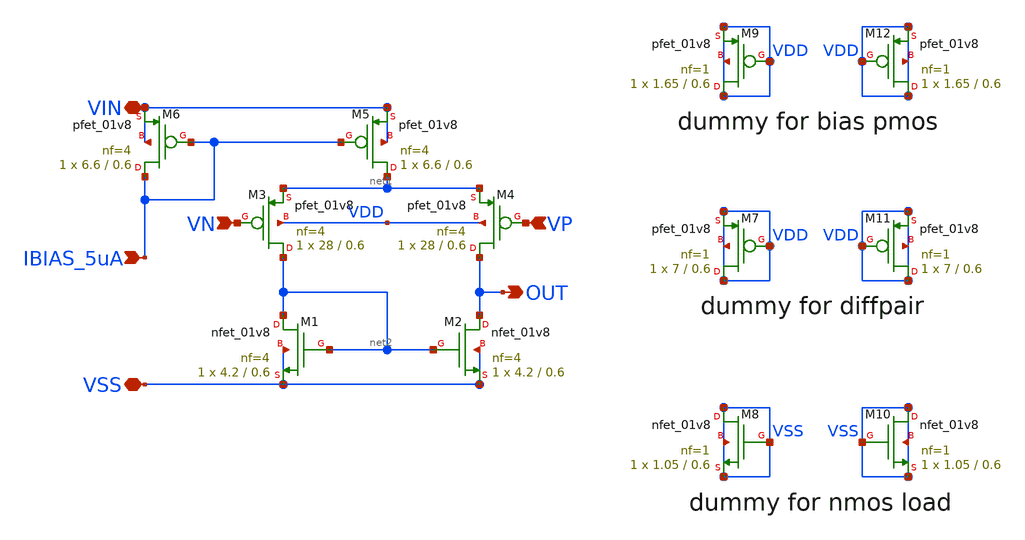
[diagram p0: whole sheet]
** sch_path: xschem/error-amplifier/error-amplifier.sch
**.subckt error-amplifier IBIAS_5uA VN VP VIN VSS OUT
*.ipin IBIAS_5uA
*.ipin VN
*.ipin VP
*.iopin VIN
*.iopin VSS
*.opin OUT
XM1 net2 net2 VSS VSS sky130_fd_pr__nfet_01v8 L=0.6 W=4.2 nf=4 ad='int((nf+1)/2) * W/nf * 0.29' as='int((nf+2)/2) * W/nf * 0.29'
+ pd='2*int((nf+1)/2) * (W/nf + 0.29)' ps='2*int((nf+2)/2) * (W/nf + 0.29)' nrd='0.29 / W' nrs='0.29 / W'
+ sa=0 sb=0 sd=0 mult=1 m=1
XM2 OUT net2 VSS VSS sky130_fd_pr__nfet_01v8 L=0.6 W=4.2 nf=4 ad='int((nf+1)/2) * W/nf * 0.29' as='int((nf+2)/2) * W/nf * 0.29'
+ pd='2*int((nf+1)/2) * (W/nf + 0.29)' ps='2*int((nf+2)/2) * (W/nf + 0.29)' nrd='0.29 / W' nrs='0.29 / W'
+ sa=0 sb=0 sd=0 mult=1 m=1
XM3 net2 VN net1 VDD sky130_fd_pr__pfet_01v8 L=0.6 W=28 nf=4 ad='int((nf+1)/2) * W/nf * 0.29' as='int((nf+2)/2) * W/nf * 0.29'
+ pd='2*int((nf+1)/2) * (W/nf + 0.29)' ps='2*int((nf+2)/2) * (W/nf + 0.29)' nrd='0.29 / W' nrs='0.29 / W'
+ sa=0 sb=0 sd=0 mult=1 m=1
XM4 OUT VP net1 VDD sky130_fd_pr__pfet_01v8 L=0.6 W=28 nf=4 ad='int((nf+1)/2) * W/nf * 0.29' as='int((nf+2)/2) * W/nf * 0.29'
+ pd='2*int((nf+1)/2) * (W/nf + 0.29)' ps='2*int((nf+2)/2) * (W/nf + 0.29)' nrd='0.29 / W' nrs='0.29 / W'
+ sa=0 sb=0 sd=0 mult=1 m=1
XM5 net1 IBIAS_5uA VIN VIN sky130_fd_pr__pfet_01v8 L=0.6 W=6.6 nf=4 ad='int((nf+1)/2) * W/nf * 0.29'
+ as='int((nf+2)/2) * W/nf * 0.29' pd='2*int((nf+1)/2) * (W/nf + 0.29)' ps='2*int((nf+2)/2) * (W/nf + 0.29)'
+ nrd='0.29 / W' nrs='0.29 / W' sa=0 sb=0 sd=0 mult=1 m=1
XM6 IBIAS_5uA IBIAS_5uA VIN VIN sky130_fd_pr__pfet_01v8 L=0.6 W=6.6 nf=4 ad='int((nf+1)/2) * W/nf * 0.29'
+ as='int((nf+2)/2) * W/nf * 0.29' pd='2*int((nf+1)/2) * (W/nf + 0.29)' ps='2*int((nf+2)/2) * (W/nf + 0.29)'
+ nrd='0.29 / W' nrs='0.29 / W' sa=0 sb=0 sd=0 mult=1 m=1
XM7 VDD VDD VDD VDD sky130_fd_pr__pfet_01v8 L=0.6 W=7 nf=1 ad='int((nf+1)/2) * W/nf * 0.29' as='int((nf+2)/2) * W/nf * 0.29'
+ pd='2*int((nf+1)/2) * (W/nf + 0.29)' ps='2*int((nf+2)/2) * (W/nf + 0.29)' nrd='0.29 / W' nrs='0.29 / W'
+ sa=0 sb=0 sd=0 mult=1 m=1
XM8 VSS VSS VSS VSS sky130_fd_pr__nfet_01v8 L=0.6 W=1.05 nf=1 ad='int((nf+1)/2) * W/nf * 0.29' as='int((nf+2)/2) * W/nf * 0.29'
+ pd='2*int((nf+1)/2) * (W/nf + 0.29)' ps='2*int((nf+2)/2) * (W/nf + 0.29)' nrd='0.29 / W' nrs='0.29 / W'
+ sa=0 sb=0 sd=0 mult=1 m=1
XM9 VDD VDD VDD VDD sky130_fd_pr__pfet_01v8 L=0.6 W=1.65 nf=1 ad='int((nf+1)/2) * W/nf * 0.29' as='int((nf+2)/2) * W/nf * 0.29'
+ pd='2*int((nf+1)/2) * (W/nf + 0.29)' ps='2*int((nf+2)/2) * (W/nf + 0.29)' nrd='0.29 / W' nrs='0.29 / W'
+ sa=0 sb=0 sd=0 mult=1 m=1
XM10 VSS VSS VSS VSS sky130_fd_pr__nfet_01v8 L=0.6 W=1.05 nf=1 ad='int((nf+1)/2) * W/nf * 0.29' as='int((nf+2)/2) * W/nf * 0.29'
+ pd='2*int((nf+1)/2) * (W/nf + 0.29)' ps='2*int((nf+2)/2) * (W/nf + 0.29)' nrd='0.29 / W' nrs='0.29 / W'
+ sa=0 sb=0 sd=0 mult=1 m=1
XM11 VDD VDD VDD VDD sky130_fd_pr__pfet_01v8 L=0.6 W=7 nf=1 ad='int((nf+1)/2) * W/nf * 0.29' as='int((nf+2)/2) * W/nf * 0.29'
+ pd='2*int((nf+1)/2) * (W/nf + 0.29)' ps='2*int((nf+2)/2) * (W/nf + 0.29)' nrd='0.29 / W' nrs='0.29 / W'
+ sa=0 sb=0 sd=0 mult=1 m=1
XM12 VDD VDD VDD VDD sky130_fd_pr__pfet_01v8 L=0.6 W=1.65 nf=1 ad='int((nf+1)/2) * W/nf * 0.29' as='int((nf+2)/2) * W/nf * 0.29'
+ pd='2*int((nf+1)/2) * (W/nf + 0.29)' ps='2*int((nf+2)/2) * (W/nf + 0.29)' nrd='0.29 / W' nrs='0.29 / W'
+ sa=0 sb=0 sd=0 mult=1 m=1
**.ends
.end
